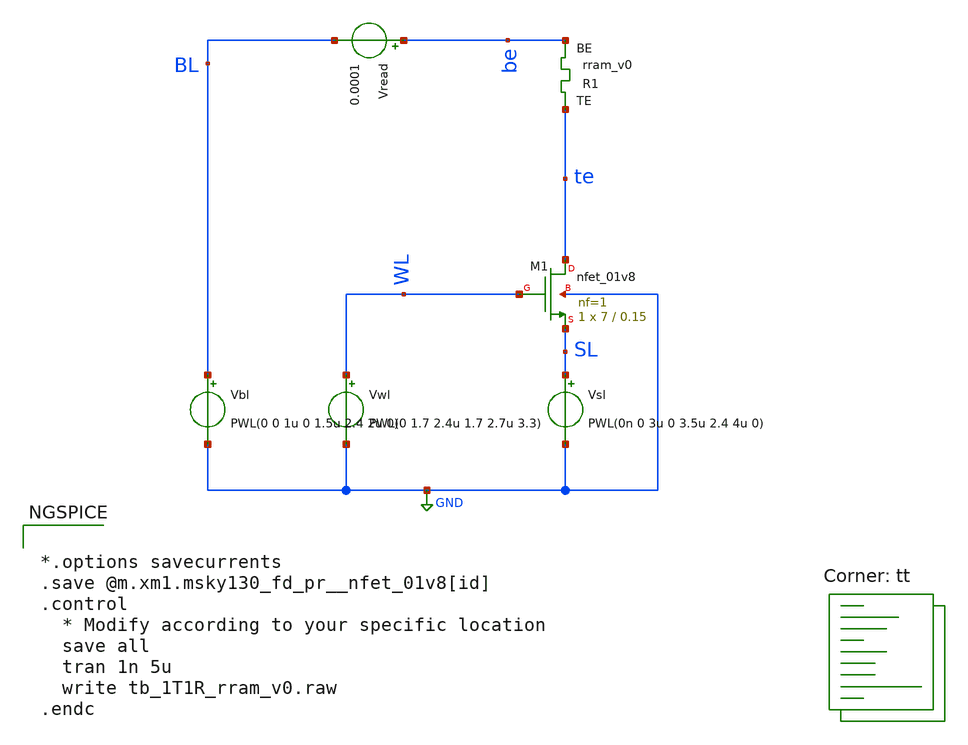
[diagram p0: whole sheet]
** sch_path: memristor_models/wellposed/tb_1T1R_rram_v0.sch
**.subckt tb_1T1R_rram_v0
XM1 te WL SL GND sky130_fd_pr__nfet_01v8 L=0.15 W=7 nf=1 ad='int((nf+1)/2) * W/nf * 0.29' as='int((nf+2)/2) * W/nf * 0.29'
+ pd='2*int((nf+1)/2) * (W/nf + 0.29)' ps='2*int((nf+2)/2) * (W/nf + 0.29)' nrd='0.29 / W' nrs='0.29 / W'
+ sa=0 sb=0 sd=0 mult=1 m=1
Vwl WL GND PWL(0 1.7 2.4u 1.7 2.7u 3.3)
Vbl BL GND PWL(0 0 1u 0 1.5u 2.4 2u 0)
Vread be BL 0.0001
Vsl SL GND PWL(0n 0 3u 0 3.5u 2.4 4u 0)
XR1 te be rram_v0
**** begin user architecture code


*.options savecurrents
.save @m.xm1.msky130_fd_pr__nfet_01v8[id]
.control
  * Modify according to your specific location
  save all
  tran 1n 5u
  write tb_1T1R_rram_v0.raw
.endc



.lib $::SKYWATER_MODELS/sky130.lib.spice tt

** opencircuitdesign pdks install
.inc $::SKYWATER_MODELS/rram_v0.spice

**** end user architecture code
**.ends
.GLOBAL GND
.end
